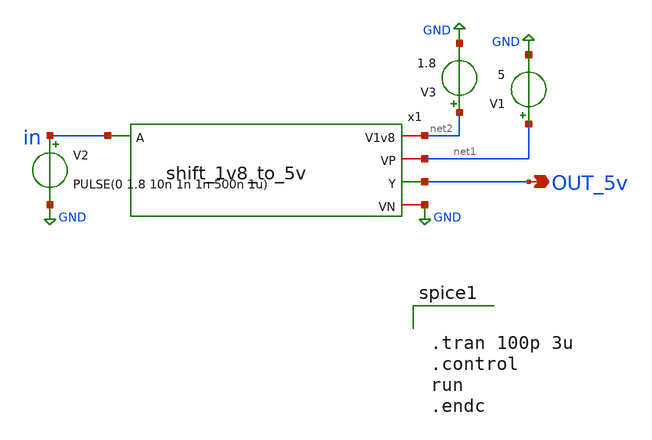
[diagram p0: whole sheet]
** sch_path: ADC/16bit_C2C/MagicAndSpice/shift_1v8_to_5v_TB.sch
**.subckt shift_1v8_to_5v_TB OUT_5v
*.opin OUT_5v
V1 net1 GND 5
V2 in GND PULSE(0 1.8 10n 1n 1n 500n 1u)
V3 net2 GND 1.8
x1 net2 net1 in OUT_5v GND shift_1v8_to_5v
**** begin user architecture code
 .lib $::SKYWATER_MODELS/sky130.lib.spice tt


.tran 100p 3u
.control
run
.endc

**** end user architecture code
**.ends

* expanding   symbol:  /home/ee431/workspace/6SAR_CDAC/shift_1v8_to_5v.sym # of pins=5
** sym_path: ADC/4bit_C2C/MagicAndSpice/shift_1v8_to_5v.sym
** sch_path: ADC/4bit_C2C/MagicAndSpice/shift_1v8_to_5v.sch
.subckt shift_1v8_to_5v V1v8 VP A Y VN
*.ipin A
*.opin Y
*.iopin VP
*.iopin VN
*.iopin V1v8
XM6 net1 A VN VN sky130_fd_pr__nfet_g5v0d10v5 L=1 W=6 nf=1 ad='int((nf+1)/2) * W/nf * 0.29' as='int((nf+2)/2) * W/nf * 0.29'
+ pd='2*int((nf+1)/2) * (W/nf + 0.29)' ps='2*int((nf+2)/2) * (W/nf + 0.29)' nrd='0.29 / W' nrs='0.29 / W'
+ sa=0 sb=0 sd=0 mult=1 m=1
XM11 net1 Y VP VP sky130_fd_pr__pfet_g5v0d10v5 L=1 W=2 nf=1 ad='int((nf+1)/2) * W/nf * 0.29' as='int((nf+2)/2) * W/nf * 0.29'
+ pd='2*int((nf+1)/2) * (W/nf + 0.29)' ps='2*int((nf+2)/2) * (W/nf + 0.29)' nrd='0.29 / W' nrs='0.29 / W'
+ sa=0 sb=0 sd=0 mult=1 m=1
XM1 Y net2 VN VN sky130_fd_pr__nfet_g5v0d10v5 L=1 W=6 nf=1 ad='int((nf+1)/2) * W/nf * 0.29' as='int((nf+2)/2) * W/nf * 0.29'
+ pd='2*int((nf+1)/2) * (W/nf + 0.29)' ps='2*int((nf+2)/2) * (W/nf + 0.29)' nrd='0.29 / W' nrs='0.29 / W'
+ sa=0 sb=0 sd=0 mult=1 m=1
XM2 Y net1 VP VP sky130_fd_pr__pfet_g5v0d10v5 L=1 W=2 nf=1 ad='int((nf+1)/2) * W/nf * 0.29' as='int((nf+2)/2) * W/nf * 0.29'
+ pd='2*int((nf+1)/2) * (W/nf + 0.29)' ps='2*int((nf+2)/2) * (W/nf + 0.29)' nrd='0.29 / W' nrs='0.29 / W'
+ sa=0 sb=0 sd=0 mult=1 m=1
XM3 net2 A VN VN sky130_fd_pr__nfet_g5v0d10v5 L=1 W=1 nf=1 ad='int((nf+1)/2) * W/nf * 0.29' as='int((nf+2)/2) * W/nf * 0.29'
+ pd='2*int((nf+1)/2) * (W/nf + 0.29)' ps='2*int((nf+2)/2) * (W/nf + 0.29)' nrd='0.29 / W' nrs='0.29 / W'
+ sa=0 sb=0 sd=0 mult=1 m=1
XM4 net2 A V1v8 V1v8 sky130_fd_pr__pfet_g5v0d10v5 L=1 W=2 nf=1 ad='int((nf+1)/2) * W/nf * 0.29' as='int((nf+2)/2) * W/nf * 0.29'
+ pd='2*int((nf+1)/2) * (W/nf + 0.29)' ps='2*int((nf+2)/2) * (W/nf + 0.29)' nrd='0.29 / W' nrs='0.29 / W'
+ sa=0 sb=0 sd=0 mult=1 m=1
.ends

.GLOBAL GND
.end
